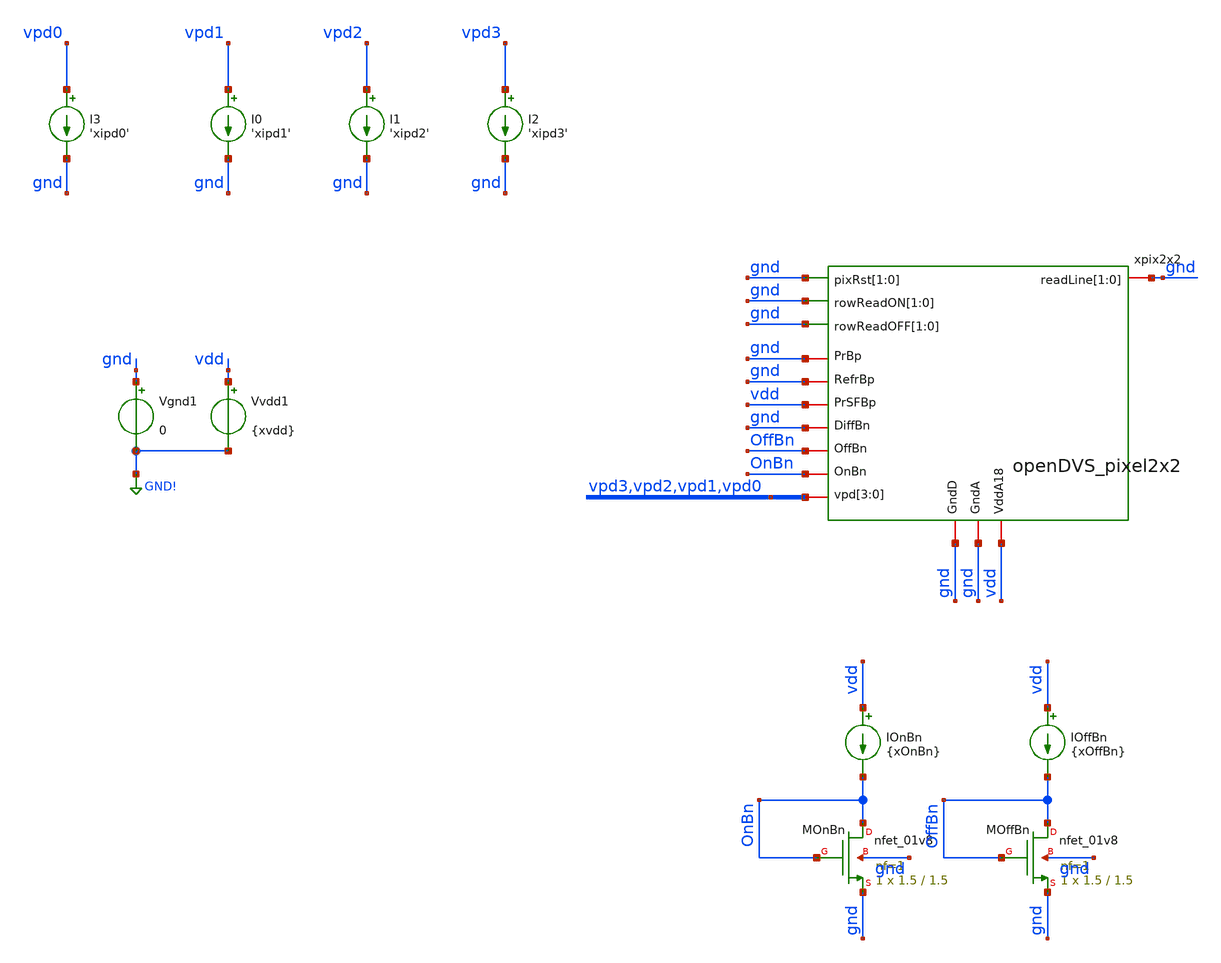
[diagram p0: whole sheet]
** sch_path: analog/klayout/production/final_merge_20260923/testbenches/cace/analog/xschem/tb_PixelComparators_dc_2x2.sch
**.subckt tb_PixelComparators_dc_2x2
XMOnBn OnBn OnBn gnd gnd sky130_fd_pr__nfet_01v8 L=1.5 W=1.5 nf=1 ad='int((1 + 1)/2) * 1.5 / 1 * 0.29'
+ as='int((1 + 2)/2) * 1.5 / 1 * 0.29' pd='2*int((1 + 1)/2) * (1.5 / 1 + 0.29)' ps='2*int((1 + 2)/2) * (1.5 / 1 + 0.29)'
+ nrd='0.29 / 1.5 ' nrs='0.29 / 1.5 ' sa=0 sb=0 sd=0 mult=1 m=1
IOnBn vdd OnBn {xOnBn}
XMOffBn OffBn OffBn gnd gnd sky130_fd_pr__nfet_01v8 L=1.5 W=1.5 nf=1 ad='int((1 + 1)/2) * 1.5 / 1 * 0.29'
+ as='int((1 + 2)/2) * 1.5 / 1 * 0.29' pd='2*int((1 + 1)/2) * (1.5 / 1 + 0.29)' ps='2*int((1 + 2)/2) * (1.5 / 1 + 0.29)'
+ nrd='0.29 / 1.5 ' nrs='0.29 / 1.5 ' sa=0 sb=0 sd=0 mult=1 m=1
IOffBn vdd OffBn {xOffBn}
Vgnd1 gnd GND! 0
Vvdd1 vdd GND! {xvdd}
xpix2x2 gnd gnd gnd gnd gnd gnd gnd gnd vpd3 vpd2 vpd1 vpd0 vdd gnd gnd OnBn OffBn gnd vdd gnd gnd
+ openDVS_pixel2x2
I0 vpd1 gnd 'xipd1'
I1 vpd2 gnd 'xipd2'
I2 vpd3 gnd 'xipd3'
I3 vpd0 gnd 'xipd0'
**** begin user architecture code

** opencircuitdesign pdks install
.lib $::SKYWATER_MODELS/sky130.lib.spice tt



.temp 27

** Set USE_PEX=1 to use extracted netlist instead of schematic
*.include /home/rpgraca/research/projects/telluride/2025/nic_eventcam/nic2025_openDVS/analog/xschem/openDVS_pixel2x2_pex_simple.spice
*.include /home/rpgraca/research/projects/telluride/2025/nic_eventcam/nic2025_openDVS/analog/xschem/openDVS_pixel2x2_pex_r.spice
*.include /home/rpgraca/research/projects/telluride/2025/nic_eventcam/nic2025_openDVS/analog/xschem/openDVS_pixel2x2_pex_cc.spice
*.include /home/rpgraca/research/projects/telluride/2025/nic_eventcam/nic2025_openDVS/analog/xschem/openDVS_pixel2x2_pex_c.spice
.include /home/rpgraca/research/projects/telluride/2025/nic_eventcam/nic2025_openDVS/analog/xschem/openDVS_pixel2x2_pex_rcc.spice
*.include /home/rpgraca/research/projects/telluride/2025/nic_eventcam/nic2025_openDVS/analog/xschem/openDVS_pixel2x2_pex_rc.spice

.option gmin=1e-16 abstol=1e-15 vntol=1e-9 reltol=1e-4 chgtol=1e-16
.option itl1=500 itl2=200
.option gminsteps=200 srcsteps=200

.param xvdd = 1.8
.param xOnBn = 200n
.param xOffBn = 0.25n
.param xvdiff = 0

.param xipd0 = 1n
.param xipd1 = 1n
.param xipd2 = 1n
.param xipd3 = 1n

** Force vdiff on Pix[0] — must be in SPICE code, not as schematic wire
** (xschem mangles dots in net labels during netlisting)
Vvdiff_pex xpix2x2.Pix[0].vdiff gnd {xvdiff}

.save all

.control
** Pass 1: coarse sweep (50mV step) to estimate thresholds
dc vvdiff_pex 0 1.8 50m
write tb_PixelComparators_dc_coarse.raw

** Pass 2 & 3: python finds thresholds, generates fine spice files, runs them
shell python3
+ /home/rpgraca/research/projects/telluride/2025/nic_eventcam/nic2025_openDVS/analog/xschem/find_comp_thresholds.py tb_PixelComparators_dc_coarse.raw tb_PixelComparators_dc_2x2.spice
.endc


**** end user architecture code
**.ends
.GLOBAL GND!
.end
